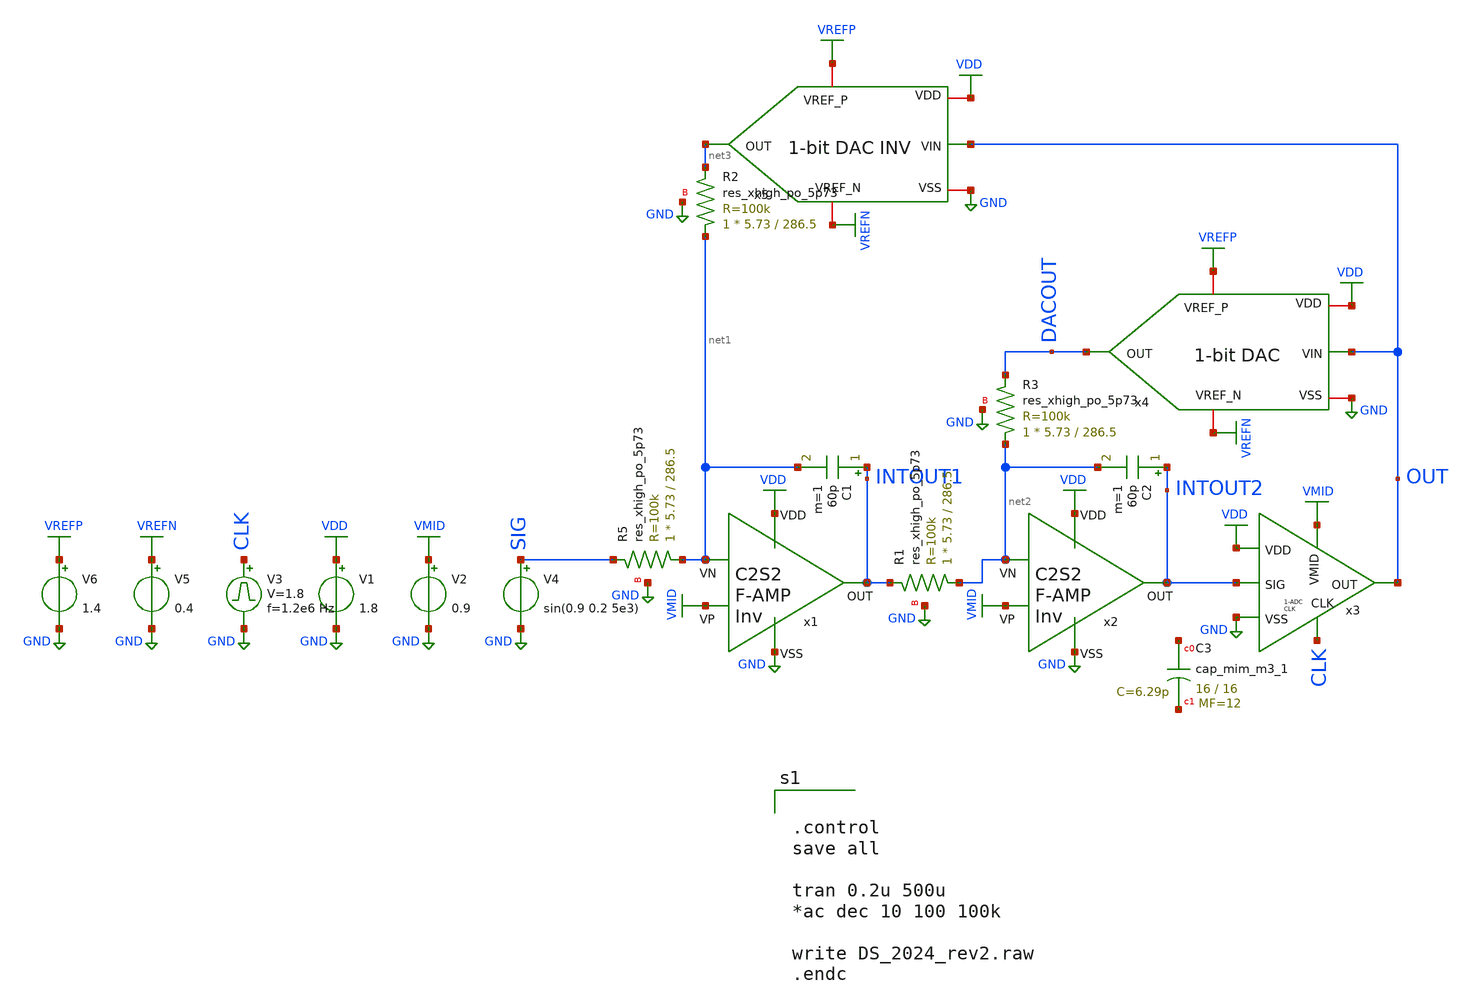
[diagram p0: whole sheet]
** sch_path: DeltaSigma/xschem/DS_2024_2p2.sch
.lib $::SKYWATER_MODELS/sky130.lib.spice tt
.include $::SKYWATER_STDCELLS/sky130_fd_sc_hd.spice

**.subckt DS_2024_2p2
V1 VDD GND 1.8
V2 VMID GND 0.9
V3 CLK GND pulse 0 1.8 '0.495/ 1.2e6 ' '0.01/1.2e6 ' '0.01/1.2e6 ' '0.49/1.2e6 ' '1/1.2e6 '
V4 SIG GND sin(0.9 0.2 5e3)
C1 INTOUT1 net1 60p m=1
C2 INTOUT2 net2 60p m=1
V5 VREFN GND 0.4
V6 VREFP GND 1.4
x1 VDD VMID net1 INTOUT1 GND C2S2_Amp_F_I
x2 VDD VMID net2 INTOUT2 GND C2S2_Amp_F_I
x5 VREFP VDD net3 OUT GND VREFN 1Bit_DAC_Inv
x4 VREFP VDD DACOUT OUT GND VREFN 1Bit_DAC
x3 VDD INTOUT2 OUT CLK GND VMID 1Bit_Clk_ADC
XR5 net1 SIG GND sky130_fd_pr__res_xhigh_po_5p73 L=286.5 mult=1 m=1
XR1 net2 INTOUT1 GND sky130_fd_pr__res_xhigh_po_5p73 L=286.5 mult=1 m=1
XR2 net1 net3 GND sky130_fd_pr__res_xhigh_po_5p73 L=286.5 mult=1 m=1
XR3 net2 DACOUT GND sky130_fd_pr__res_xhigh_po_5p73 L=286.5 mult=1 m=1
XC3 net4 net5 sky130_fd_pr__cap_mim_m3_1 W=16 L=16 MF=12 m=12
**** begin user architecture code


.control
save all

tran 0.2u 500u
*ac dec 10 100 100k

write DS_2024_rev2.raw
.endc


**** end user architecture code
**.ends
.GLOBAL VDD
.GLOBAL GND
.GLOBAL VMID
.GLOBAL VREFN
.GLOBAL VREFP
.end
